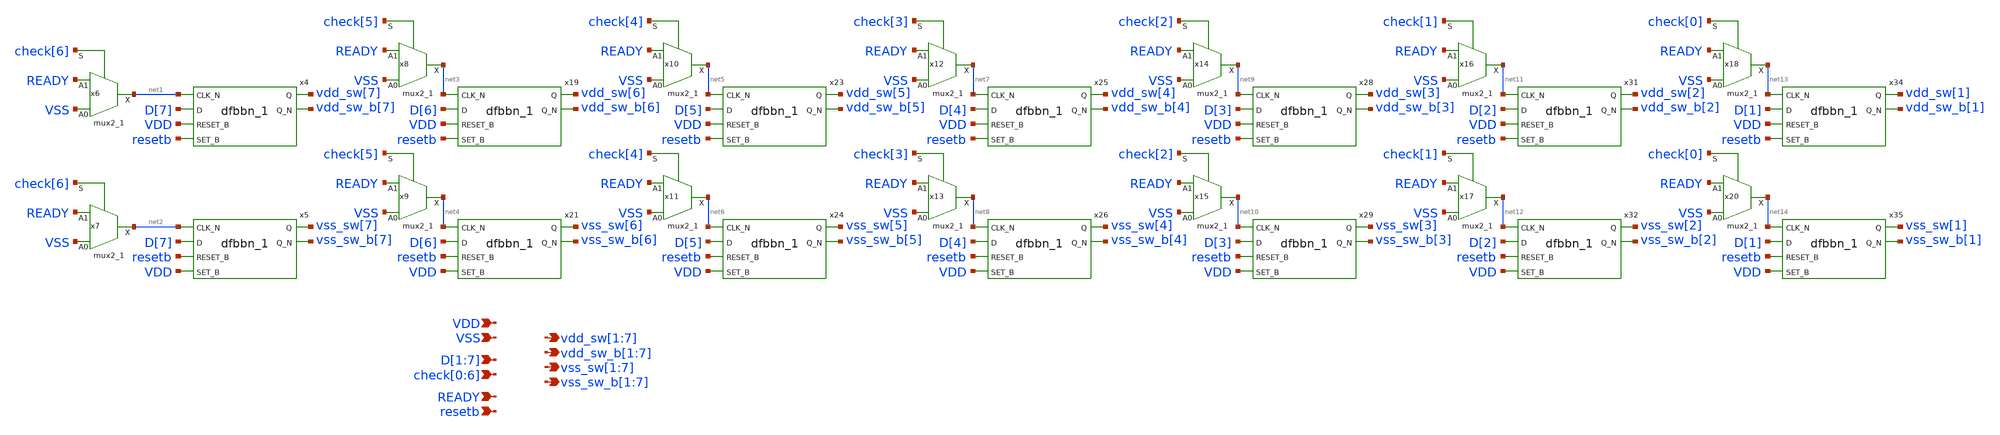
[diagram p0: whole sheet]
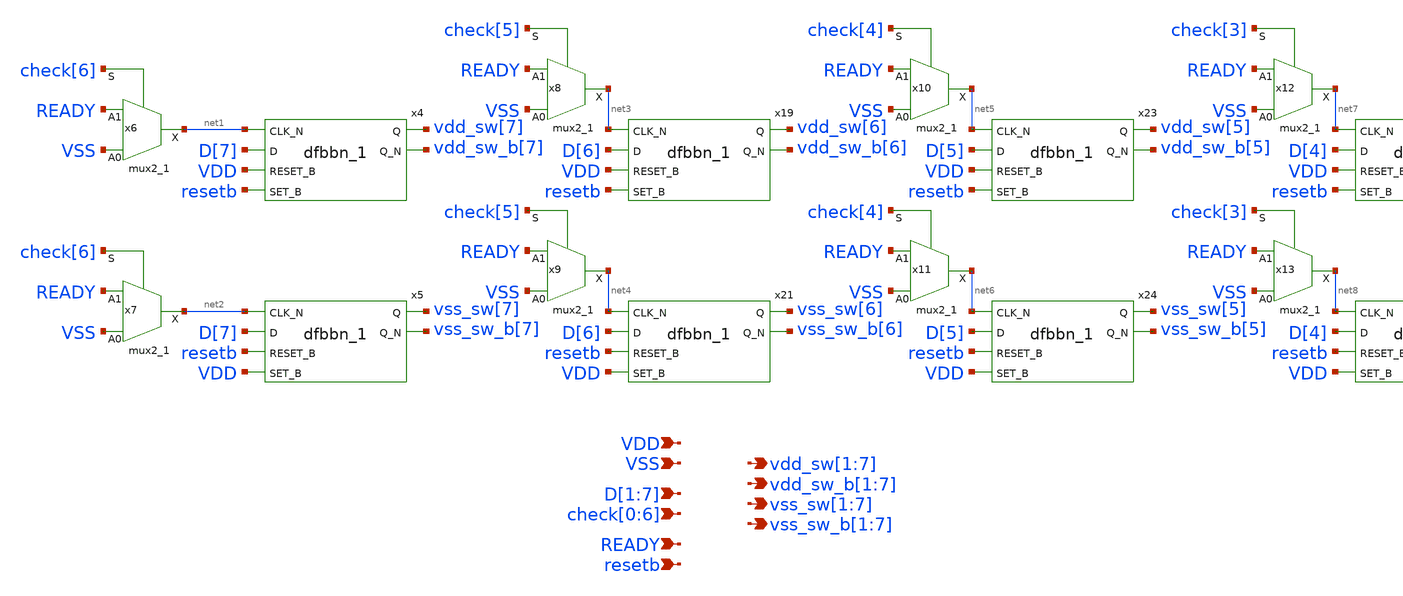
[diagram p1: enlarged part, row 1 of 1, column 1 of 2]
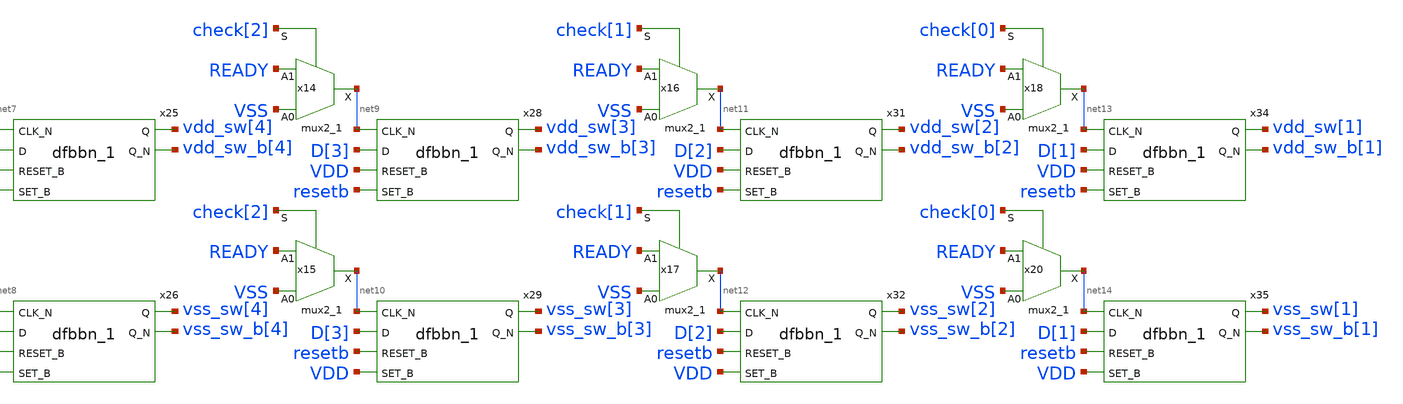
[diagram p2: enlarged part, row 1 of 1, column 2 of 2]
** sch_path: hgu/xschem/hgu_sarlogic_sw_ctrl.sch
**.subckt hgu_sarlogic_sw_ctrl vdd_sw[1],vdd_sw[2],vdd_sw[3],vdd_sw[4],vdd_sw[5],vdd_sw[6],vdd_sw[7]
*+ vdd_sw_b[1],vdd_sw_b[2],vdd_sw_b[3],vdd_sw_b[4],vdd_sw_b[5],vdd_sw_b[6],vdd_sw_b[7] vss_sw[1],vss_sw[2],vss_sw[3],vss_sw[4],vss_sw[5],vss_sw[6],vss_sw[7]
*+ vss_sw_b[1],vss_sw_b[2],vss_sw_b[3],vss_sw_b[4],vss_sw_b[5],vss_sw_b[6],vss_sw_b[7] VDD VSS READY D[1],D[2],D[3],D[4],D[5],D[6],D[7]
*+ check[0],check[1],check[2],check[3],check[4],check[5],check[6] resetb
*.opin vdd_sw[1],vdd_sw[2],vdd_sw[3],vdd_sw[4],vdd_sw[5],vdd_sw[6],vdd_sw[7]
*.opin vdd_sw_b[1],vdd_sw_b[2],vdd_sw_b[3],vdd_sw_b[4],vdd_sw_b[5],vdd_sw_b[6],vdd_sw_b[7]
*.opin vss_sw[1],vss_sw[2],vss_sw[3],vss_sw[4],vss_sw[5],vss_sw[6],vss_sw[7]
*.opin vss_sw_b[1],vss_sw_b[2],vss_sw_b[3],vss_sw_b[4],vss_sw_b[5],vss_sw_b[6],vss_sw_b[7]
*.ipin VDD
*.ipin VSS
*.ipin READY
*.ipin D[1],D[2],D[3],D[4],D[5],D[6],D[7]
*.ipin check[0],check[1],check[2],check[3],check[4],check[5],check[6]
*.ipin resetb
x4 net1 D[7] VDD resetb VGND VNB VPB VPWR vdd_sw[7] vdd_sw_b[7] sky130_fd_sc_hd__dfbbn_1
x5 net2 D[7] resetb VDD VGND VNB VPB VPWR vss_sw[7] vss_sw_b[7] sky130_fd_sc_hd__dfbbn_1
x19 net3 D[6] VDD resetb VGND VNB VPB VPWR vdd_sw[6] vdd_sw_b[6] sky130_fd_sc_hd__dfbbn_1
x21 net4 D[6] resetb VDD VGND VNB VPB VPWR vss_sw[6] vss_sw_b[6] sky130_fd_sc_hd__dfbbn_1
x23 net5 D[5] VDD resetb VGND VNB VPB VPWR vdd_sw[5] vdd_sw_b[5] sky130_fd_sc_hd__dfbbn_1
x24 net6 D[5] resetb VDD VGND VNB VPB VPWR vss_sw[5] vss_sw_b[5] sky130_fd_sc_hd__dfbbn_1
x25 net7 D[4] VDD resetb VGND VNB VPB VPWR vdd_sw[4] vdd_sw_b[4] sky130_fd_sc_hd__dfbbn_1
x26 net8 D[4] resetb VDD VGND VNB VPB VPWR vss_sw[4] vss_sw_b[4] sky130_fd_sc_hd__dfbbn_1
x28 net9 D[3] VDD resetb VGND VNB VPB VPWR vdd_sw[3] vdd_sw_b[3] sky130_fd_sc_hd__dfbbn_1
x29 net10 D[3] resetb VDD VGND VNB VPB VPWR vss_sw[3] vss_sw_b[3] sky130_fd_sc_hd__dfbbn_1
x31 net11 D[2] VDD resetb VGND VNB VPB VPWR vdd_sw[2] vdd_sw_b[2] sky130_fd_sc_hd__dfbbn_1
x32 net12 D[2] resetb VDD VGND VNB VPB VPWR vss_sw[2] vss_sw_b[2] sky130_fd_sc_hd__dfbbn_1
x34 net13 D[1] VDD resetb VGND VNB VPB VPWR vdd_sw[1] vdd_sw_b[1] sky130_fd_sc_hd__dfbbn_1
x35 net14 D[1] resetb VDD VGND VNB VPB VPWR vss_sw[1] vss_sw_b[1] sky130_fd_sc_hd__dfbbn_1
x6 VSS READY check[6] VGND VNB VPB VPWR net1 sky130_fd_sc_hd__mux2_1
x7 VSS READY check[6] VGND VNB VPB VPWR net2 sky130_fd_sc_hd__mux2_1
x8 VSS READY check[5] VGND VNB VPB VPWR net3 sky130_fd_sc_hd__mux2_1
x9 VSS READY check[5] VGND VNB VPB VPWR net4 sky130_fd_sc_hd__mux2_1
x10 VSS READY check[4] VGND VNB VPB VPWR net5 sky130_fd_sc_hd__mux2_1
x11 VSS READY check[4] VGND VNB VPB VPWR net6 sky130_fd_sc_hd__mux2_1
x12 VSS READY check[3] VGND VNB VPB VPWR net7 sky130_fd_sc_hd__mux2_1
x13 VSS READY check[3] VGND VNB VPB VPWR net8 sky130_fd_sc_hd__mux2_1
x14 VSS READY check[2] VGND VNB VPB VPWR net9 sky130_fd_sc_hd__mux2_1
x15 VSS READY check[2] VGND VNB VPB VPWR net10 sky130_fd_sc_hd__mux2_1
x16 VSS READY check[1] VGND VNB VPB VPWR net11 sky130_fd_sc_hd__mux2_1
x17 VSS READY check[1] VGND VNB VPB VPWR net12 sky130_fd_sc_hd__mux2_1
x18 VSS READY check[0] VGND VNB VPB VPWR net13 sky130_fd_sc_hd__mux2_1
x20 VSS READY check[0] VGND VNB VPB VPWR net14 sky130_fd_sc_hd__mux2_1
**.ends
.end
